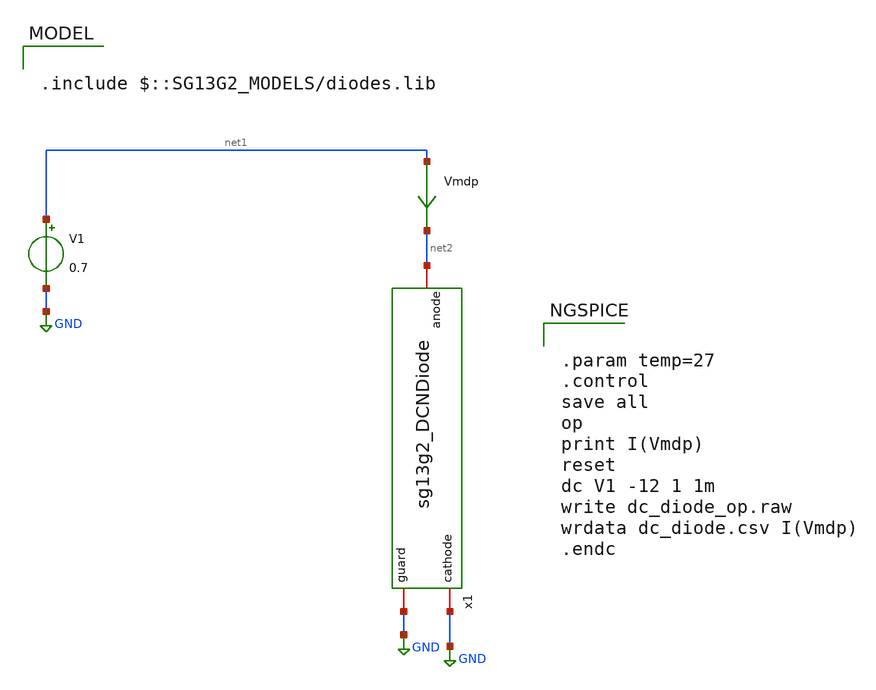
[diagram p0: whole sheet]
** sch_path: ihp-sg13g2/libs.tech/xschem/sg13g2_tests/dc_diode_op.sch
* Copyright 2023 IHP PDK Authors
**.subckt dc_diode_op
V1 net1 GND 0.7
Vmdp net1 net2 0
.save i(vmdp)
x1 GND net2 GND sg13g2_DCNDiode
**** begin user architecture code

.include $::SG13G2_MODELS/diodes.lib



.param temp=27
.control
save all
op
print I(Vmdp)
reset
dc V1 -12 1 1m
write dc_diode_op.raw
wrdata dc_diode.csv I(Vmdp)
.endc


**** end user architecture code
**.ends

* expanding   symbol:  sg13g2_DCNDiode.sym # of pins=3
** sym_path: ihp-sg13g2/libs.ref/sg13g2_io/xschem/sg13g2_DCNDiode.sym
** sch_path: ihp-sg13g2/libs.ref/sg13g2_io/xschem/sg13g2_DCNDiode.sch
.subckt sg13g2_DCNDiode cathode anode guard
*.iopin cathode
*.iopin anode
*.iopin guard
XD1 anode cathode dantenna l=1.26u w=27.78u
XD2 anode cathode dantenna l=1.26u w=27.78u
.ends

.GLOBAL GND
.end
